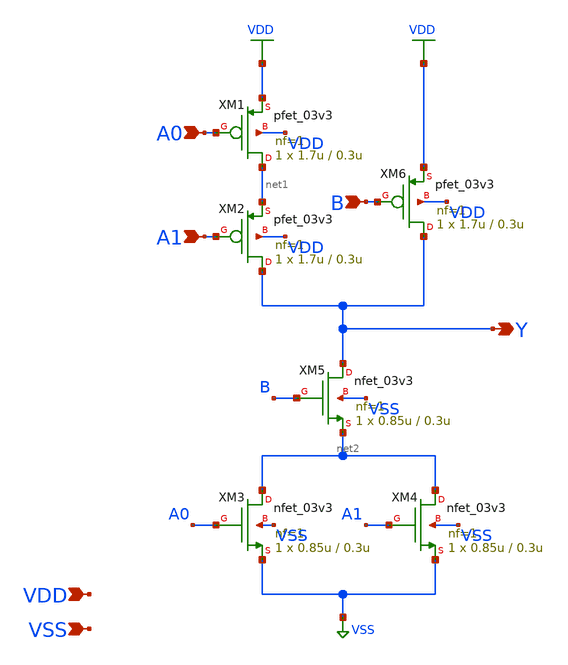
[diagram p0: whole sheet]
** sch_path: gf180mcu_osu_sc_gp12t3v3/xschem/gf180mcu_osu_sc_gp12t3v3__oai21_1.sch
**.subckt gf180mcu_osu_sc_gp12t3v3__oai21_1 A0 A1 B Y VDD VSS
*.ipin A0
*.ipin A1
*.ipin B
*.opin Y
*.ipin VDD
*.ipin VSS
XM1 net1 A0 VDD VDD pfet_03v3 L=0.3u W=1.7u nf=1 ad='int((nf+1)/2) * W/nf * 0.18u' as='int((nf+2)/2) * W/nf * 0.18u'
+ pd='2*int((nf+1)/2) * (W/nf + 0.18u)' ps='2*int((nf+2)/2) * (W/nf + 0.18u)' nrd='0.18u / W' nrs='0.18u / W'
+ sa=0 sb=0 sd=0 m=1
XM2 Y A1 net1 VDD pfet_03v3 L=0.3u W=1.7u nf=1 ad='int((nf+1)/2) * W/nf * 0.18u' as='int((nf+2)/2) * W/nf * 0.18u'
+ pd='2*int((nf+1)/2) * (W/nf + 0.18u)' ps='2*int((nf+2)/2) * (W/nf + 0.18u)' nrd='0.18u / W' nrs='0.18u / W'
+ sa=0 sb=0 sd=0 m=1
XM3 net2 A0 VSS VSS nfet_03v3 L=0.3u W=0.85u nf=1 ad='int((nf+1)/2) * W/nf * 0.18u' as='int((nf+2)/2) * W/nf * 0.18u'
+ pd='2*int((nf+1)/2) * (W/nf + 0.18u)' ps='2*int((nf+2)/2) * (W/nf + 0.18u)' nrd='0.18u / W' nrs='0.18u / W'
+ sa=0 sb=0 sd=0 m=1
XM4 net2 A1 VSS VSS nfet_03v3 L=0.3u W=0.85u nf=1 ad='int((nf+1)/2) * W/nf * 0.18u' as='int((nf+2)/2) * W/nf * 0.18u'
+ pd='2*int((nf+1)/2) * (W/nf + 0.18u)' ps='2*int((nf+2)/2) * (W/nf + 0.18u)' nrd='0.18u / W' nrs='0.18u / W'
+ sa=0 sb=0 sd=0 m=1
XM5 Y B net2 VSS nfet_03v3 L=0.3u W=0.85u nf=1 ad='int((nf+1)/2) * W/nf * 0.18u' as='int((nf+2)/2) * W/nf * 0.18u'
+ pd='2*int((nf+1)/2) * (W/nf + 0.18u)' ps='2*int((nf+2)/2) * (W/nf + 0.18u)' nrd='0.18u / W' nrs='0.18u / W'
+ sa=0 sb=0 sd=0 m=1
XM6 Y B VDD VDD pfet_03v3 L=0.3u W=1.7u nf=1 ad='int((nf+1)/2) * W/nf * 0.18u' as='int((nf+2)/2) * W/nf * 0.18u'
+ pd='2*int((nf+1)/2) * (W/nf + 0.18u)' ps='2*int((nf+2)/2) * (W/nf + 0.18u)' nrd='0.18u / W' nrs='0.18u / W'
+ sa=0 sb=0 sd=0 m=1
**.ends
.GLOBAL VDD
.GLOBAL VSS
.end
